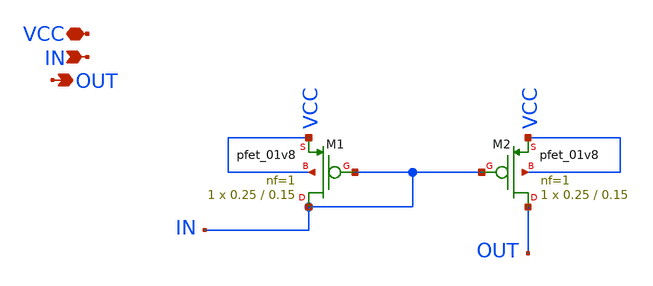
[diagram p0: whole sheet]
** sch_path: xschem/cm.sch
**.subckt cm VCC IN OUT
*.iopin VCC
*.ipin IN
*.opin OUT
XM1 IN IN VCC VCC sky130_fd_pr__pfet_01v8 L=0.15 W=0.25 nf=1 ad='int((nf+1)/2) * W/nf * 0.29' as='int((nf+2)/2) * W/nf * 0.29'
+ pd='2*int((nf+1)/2) * (W/nf + 0.29)' ps='2*int((nf+2)/2) * (W/nf + 0.29)' nrd='0.29 / W' nrs='0.29 / W'
+ sa=0 sb=0 sd=0 mult=1 m=1
XM2 OUT IN VCC VCC sky130_fd_pr__pfet_01v8 L=0.15 W=0.25 nf=1 ad='int((nf+1)/2) * W/nf * 0.29' as='int((nf+2)/2) * W/nf * 0.29'
+ pd='2*int((nf+1)/2) * (W/nf + 0.29)' ps='2*int((nf+2)/2) * (W/nf + 0.29)' nrd='0.29 / W' nrs='0.29 / W'
+ sa=0 sb=0 sd=0 mult=1 m=1
**.ends
.end
